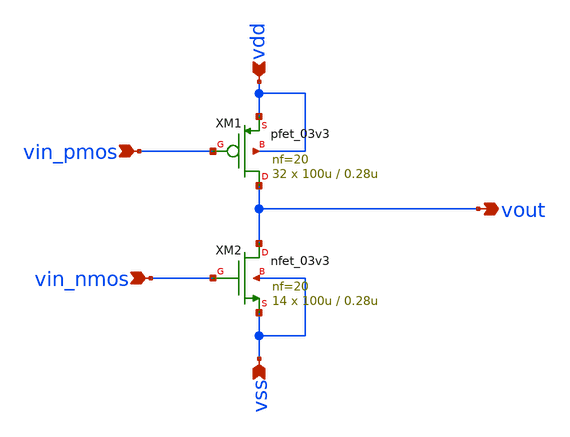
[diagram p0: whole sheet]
** sch_path: designs/libs/core_analog/Output_Stage/Output_Stage.sch
**.subckt Output_Stage vin_pmos vdd vss vout vin_nmos
*.ipin vin_pmos
*.ipin vdd
*.ipin vss
*.opin vout
*.ipin vin_nmos
XM1 vout vin_pmos vdd vdd pfet_03v3 L=0.28u W=100u nf=20 ad='int((nf+1)/2) * W/nf * 0.18u' as='int((nf+2)/2) * W/nf * 0.18u'
+ pd='2*int((nf+1)/2) * (W/nf + 0.18u)' ps='2*int((nf+2)/2) * (W/nf + 0.18u)' nrd='0.18u / W' nrs='0.18u / W'
+ sa=0 sb=0 sd=0 m=32
XM2 vout vin_nmos vss vss nfet_03v3 L=0.28u W=100u nf=20 ad='int((nf+1)/2) * W/nf * 0.18u' as='int((nf+2)/2) * W/nf * 0.18u'
+ pd='2*int((nf+1)/2) * (W/nf + 0.18u)' ps='2*int((nf+2)/2) * (W/nf + 0.18u)' nrd='0.18u / W' nrs='0.18u / W'
+ sa=0 sb=0 sd=0 m=14
**.ends
.end
